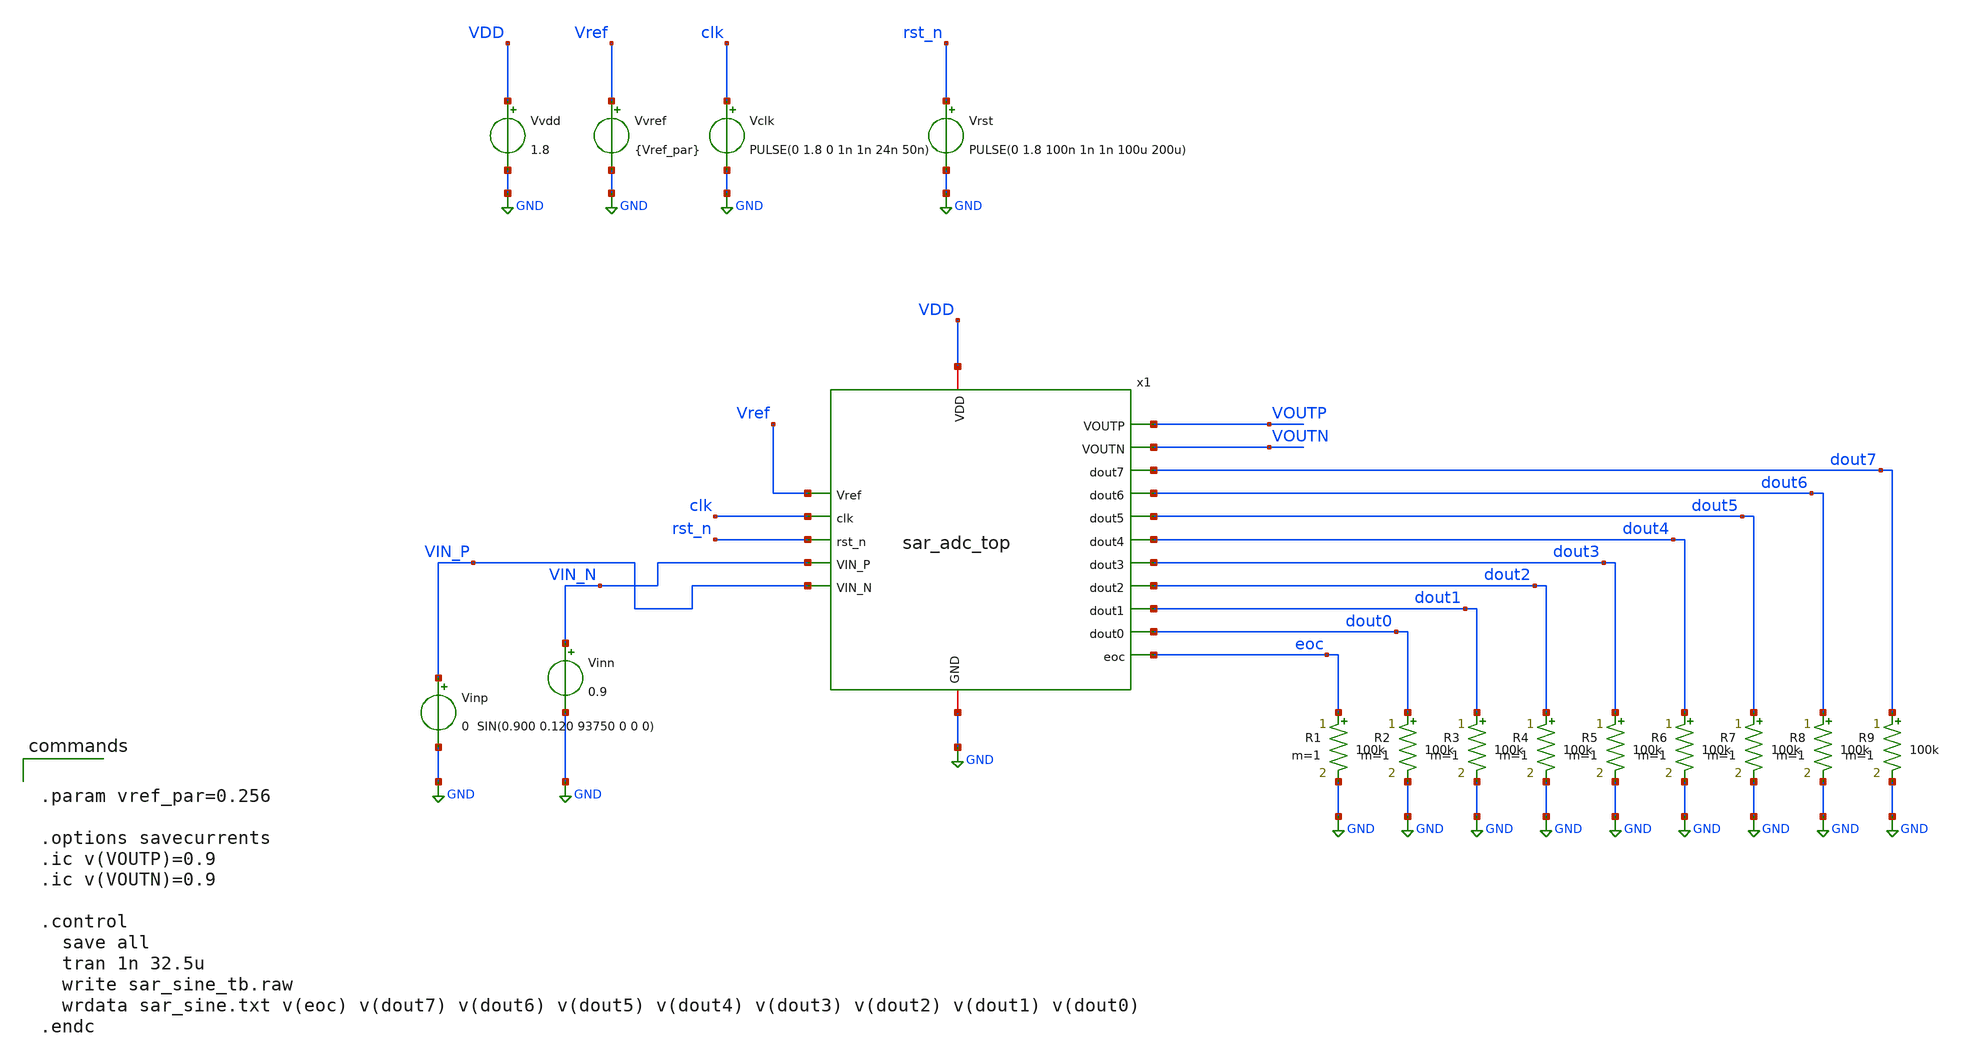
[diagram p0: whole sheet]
** sch_path: 05_mixed_signal/soluzioni/lab03/xschem/sar_sine_tb.sch
**.subckt sar_sine_tb
x1 VDD GND Vref VOUTP VOUTN clk rst_n VIN_N dout7 dout6 dout5 dout4 dout3 dout2 dout1 dout0 VIN_P
+ eoc sar_adc_top
Vvdd VDD GND 1.8
Vvref Vref GND {Vref_par}
Vclk clk GND PULSE(0 1.8 0 1n 1n 24n 50n)
Vrst rst_n GND PULSE(0 1.8 100n 1n 1n 100u 200u)
R1 eoc GND 100k m=1
R2 dout0 GND 100k m=1
R3 dout1 GND 100k m=1
R4 dout2 GND 100k m=1
R5 dout3 GND 100k m=1
R6 dout4 GND 100k m=1
R7 dout5 GND 100k m=1
R8 dout6 GND 100k m=1
R9 dout7 GND 100k m=1
Vinp VIN_P GND 0 SIN(0.900 0.120 93750 0 0 0)
Vinn VIN_N GND 0.9
**** begin user architecture code

** opencircuitdesign pdks install
.lib $::SKYWATER_MODELS/sky130.lib.spice tt



.param vref_par=0.256

.options savecurrents
.ic v(VOUTP)=0.9
.ic v(VOUTN)=0.9

.control
  save all
  tran 1n 32.5u
  write sar_sine_tb.raw
  wrdata sar_sine.txt v(eoc) v(dout7) v(dout6) v(dout5) v(dout4) v(dout3) v(dout2) v(dout1) v(dout0)
.endc


**** end user architecture code
**.ends
.GLOBAL GND
.end
